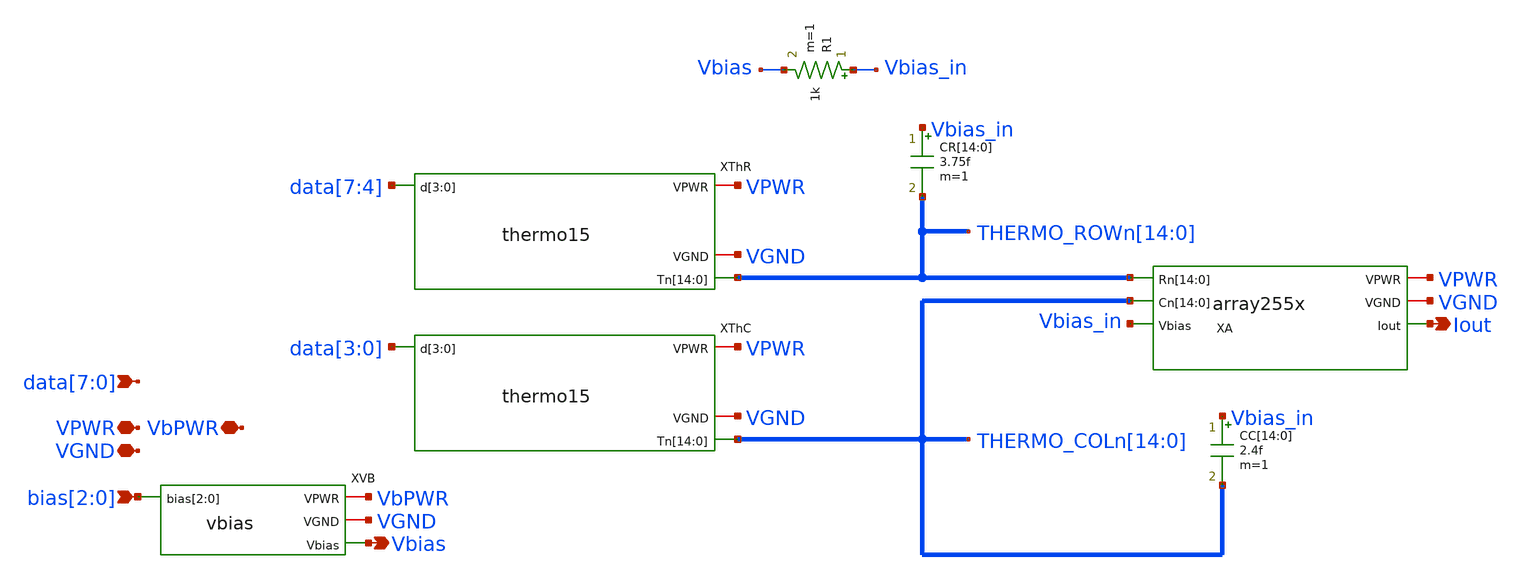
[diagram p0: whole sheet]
** sch_path: xschem/csdac255.sch
**.subckt csdac255 VPWR Iout VGND bias[2],bias[1],bias[0]
*+ data[7],data[6],data[5],data[4],data[3],data[2],data[1],data[0] VbPWR Vbias
*.iopin VPWR
*.opin Iout
*.iopin VGND
*.ipin bias[2],bias[1],bias[0]
*.ipin data[7],data[6],data[5],data[4],data[3],data[2],data[1],data[0]
*.iopin VbPWR
*.opin Vbias
XThR VPWR VGND THERMO_ROWn[14] THERMO_ROWn[13] THERMO_ROWn[12] THERMO_ROWn[11] THERMO_ROWn[10]
+ THERMO_ROWn[9] THERMO_ROWn[8] THERMO_ROWn[7] THERMO_ROWn[6] THERMO_ROWn[5] THERMO_ROWn[4] THERMO_ROWn[3]
+ THERMO_ROWn[2] THERMO_ROWn[1] THERMO_ROWn[0] data[7] data[6] data[5] data[4] thermo15
XA VPWR VGND THERMO_ROWn[14] THERMO_ROWn[13] THERMO_ROWn[12] THERMO_ROWn[11] THERMO_ROWn[10]
+ THERMO_ROWn[9] THERMO_ROWn[8] THERMO_ROWn[7] THERMO_ROWn[6] THERMO_ROWn[5] THERMO_ROWn[4] THERMO_ROWn[3]
+ THERMO_ROWn[2] THERMO_ROWn[1] THERMO_ROWn[0] THERMO_COLn[14] THERMO_COLn[13] THERMO_COLn[12] THERMO_COLn[11]
+ THERMO_COLn[10] THERMO_COLn[9] THERMO_COLn[8] THERMO_COLn[7] THERMO_COLn[6] THERMO_COLn[5] THERMO_COLn[4]
+ THERMO_COLn[3] THERMO_COLn[2] THERMO_COLn[1] THERMO_COLn[0] Vbias_in Iout array255x
XThC VPWR VGND THERMO_COLn[14] THERMO_COLn[13] THERMO_COLn[12] THERMO_COLn[11] THERMO_COLn[10]
+ THERMO_COLn[9] THERMO_COLn[8] THERMO_COLn[7] THERMO_COLn[6] THERMO_COLn[5] THERMO_COLn[4] THERMO_COLn[3]
+ THERMO_COLn[2] THERMO_COLn[1] THERMO_COLn[0] data[3] data[2] data[1] data[0] thermo15
CR[14] Vbias_in THERMO_ROWn[14] 3.75f m=1
CR[13] Vbias_in THERMO_ROWn[13] 3.75f m=1
CR[12] Vbias_in THERMO_ROWn[12] 3.75f m=1
CR[11] Vbias_in THERMO_ROWn[11] 3.75f m=1
CR[10] Vbias_in THERMO_ROWn[10] 3.75f m=1
CR[9] Vbias_in THERMO_ROWn[9] 3.75f m=1
CR[8] Vbias_in THERMO_ROWn[8] 3.75f m=1
CR[7] Vbias_in THERMO_ROWn[7] 3.75f m=1
CR[6] Vbias_in THERMO_ROWn[6] 3.75f m=1
CR[5] Vbias_in THERMO_ROWn[5] 3.75f m=1
CR[4] Vbias_in THERMO_ROWn[4] 3.75f m=1
CR[3] Vbias_in THERMO_ROWn[3] 3.75f m=1
CR[2] Vbias_in THERMO_ROWn[2] 3.75f m=1
CR[1] Vbias_in THERMO_ROWn[1] 3.75f m=1
CR[0] Vbias_in THERMO_ROWn[0] 3.75f m=1
CC[14] Vbias_in THERMO_COLn[14] 2.4f m=1
CC[13] Vbias_in THERMO_COLn[13] 2.4f m=1
CC[12] Vbias_in THERMO_COLn[12] 2.4f m=1
CC[11] Vbias_in THERMO_COLn[11] 2.4f m=1
CC[10] Vbias_in THERMO_COLn[10] 2.4f m=1
CC[9] Vbias_in THERMO_COLn[9] 2.4f m=1
CC[8] Vbias_in THERMO_COLn[8] 2.4f m=1
CC[7] Vbias_in THERMO_COLn[7] 2.4f m=1
CC[6] Vbias_in THERMO_COLn[6] 2.4f m=1
CC[5] Vbias_in THERMO_COLn[5] 2.4f m=1
CC[4] Vbias_in THERMO_COLn[4] 2.4f m=1
CC[3] Vbias_in THERMO_COLn[3] 2.4f m=1
CC[2] Vbias_in THERMO_COLn[2] 2.4f m=1
CC[1] Vbias_in THERMO_COLn[1] 2.4f m=1
CC[0] Vbias_in THERMO_COLn[0] 2.4f m=1
XVB VbPWR VGND bias[2] bias[1] bias[0] Vbias vbias
R1 Vbias_in Vbias 1k m=1
**.ends
.end
